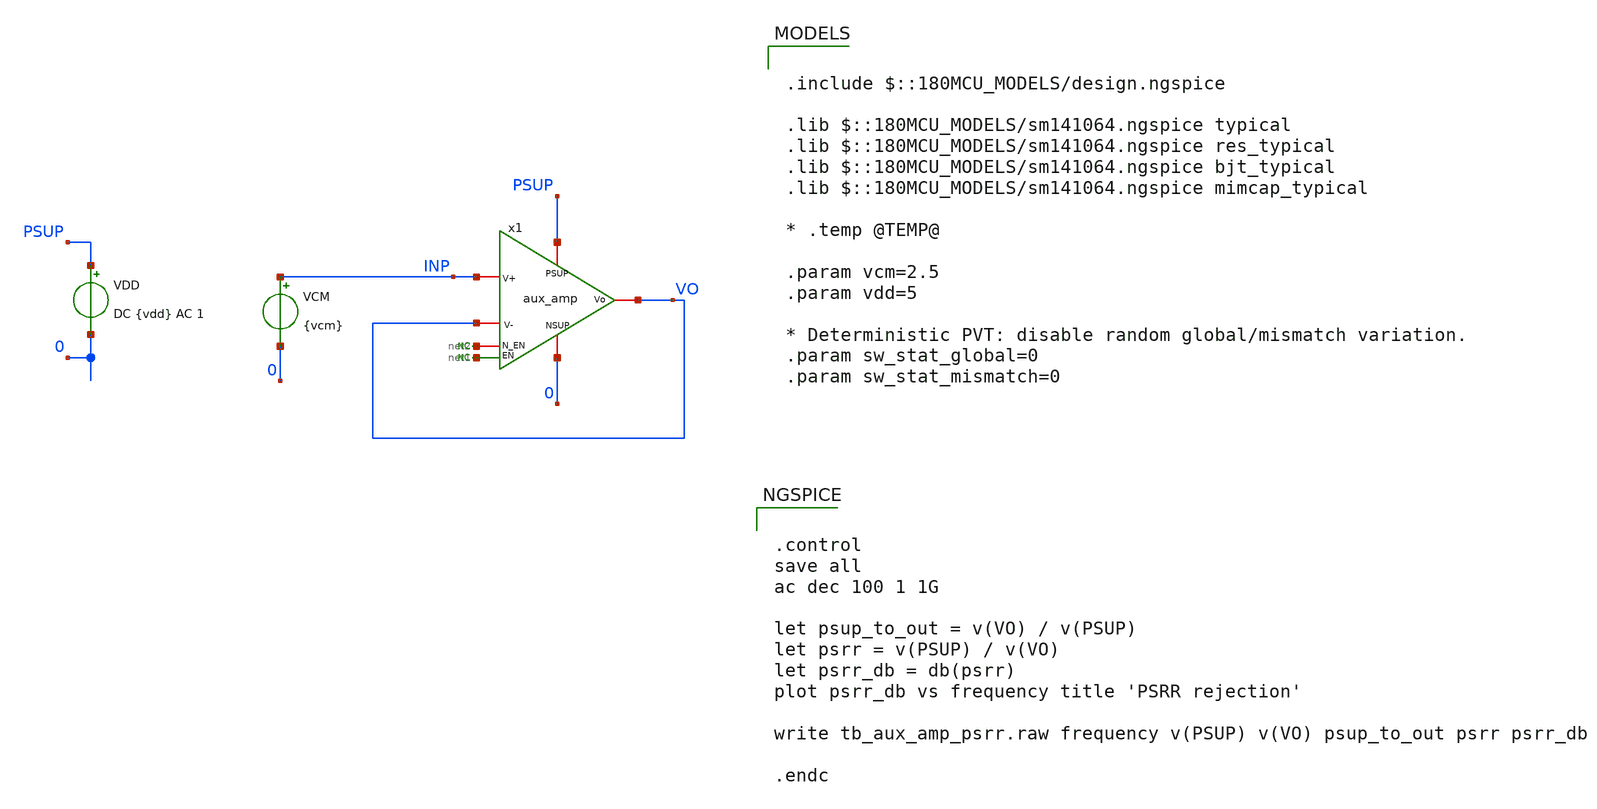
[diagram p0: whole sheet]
** sch_path: xschem/blocks/error_amp/tb_aux_amp_psrr.sch
**.subckt tb_aux_amp_psrr
VDD PSUP 0 DC {vdd} AC 1
VCM INP 0 {vcm}
* noconn #net1
* noconn #net2
x1 PSUP VO INP VO net2 0 net1 aux_amp
**** begin user architecture code

.include $::180MCU_MODELS/design.ngspice

.lib $::180MCU_MODELS/sm141064.ngspice typical
.lib $::180MCU_MODELS/sm141064.ngspice res_typical
.lib $::180MCU_MODELS/sm141064.ngspice bjt_typical
.lib $::180MCU_MODELS/sm141064.ngspice mimcap_typical

* .temp @TEMP@

.param vcm=2.5
.param vdd=5

* Deterministic PVT: disable random global/mismatch variation.
.param sw_stat_global=0
.param sw_stat_mismatch=0



.control
save all
ac dec 100 1 1G

let psup_to_out = v(VO) / v(PSUP)
let psrr = v(PSUP) / v(VO)
let psrr_db = db(psrr)
plot psrr_db vs frequency title 'PSRR rejection'

write tb_aux_amp_psrr.raw frequency v(PSUP) v(VO) psup_to_out psrr psrr_db

.endc


**** end user architecture code
**.ends

* expanding   symbol:  blocks/aux_amp/aux_amp.sym # of pins=7
** sym_path: xschem/lib/aux_amp.sym
** sch_path: xschem/lib/aux_amp.sch
.subckt aux_amp PSUP Vo V+ V- N_EN NSUP EN
*.ipin PSUP
*.ipin NSUP
*.ipin N_EN
*.ipin EN
*.ipin V+
*.ipin V-
*.opin Vo
XM1 Vo V- net2 net2 nfet_06v0 L=1.80u W=0.80u nf=1 ad='int((nf+1)/2) * W/nf * 0.18u' as='int((nf+2)/2) * W/nf * 0.18u'
+ pd='2*int((nf+1)/2) * (W/nf + 0.18u)' ps='2*int((nf+2)/2) * (W/nf + 0.18u)' nrd='0.18u / W' nrs='0.18u / W'
+ sa=0 sb=0 sd=0 m=1
XM2 net1 V+ net2 net2 nfet_06v0 L=1.80u W=0.80u nf=1 ad='int((nf+1)/2) * W/nf * 0.18u' as='int((nf+2)/2) * W/nf * 0.18u'
+ pd='2*int((nf+1)/2) * (W/nf + 0.18u)' ps='2*int((nf+2)/2) * (W/nf + 0.18u)' nrd='0.18u / W' nrs='0.18u / W'
+ sa=0 sb=0 sd=0 m=1
XM5 net1 net1 PSUP PSUP pfet_06v0 L=0.55u W=0.30u nf=1 ad='int((nf+1)/2) * W/nf * 0.18u' as='int((nf+2)/2) * W/nf * 0.18u'
+ pd='2*int((nf+1)/2) * (W/nf + 0.18u)' ps='2*int((nf+2)/2) * (W/nf + 0.18u)' nrd='0.18u / W' nrs='0.18u / W'
+ sa=0 sb=0 sd=0 m=1
XM6 Vo net1 PSUP PSUP pfet_06v0 L=0.55u W=0.30u nf=1 ad='int((nf+1)/2) * W/nf * 0.18u' as='int((nf+2)/2) * W/nf * 0.18u'
+ pd='2*int((nf+1)/2) * (W/nf + 0.18u)' ps='2*int((nf+2)/2) * (W/nf + 0.18u)' nrd='0.18u / W' nrs='0.18u / W'
+ sa=0 sb=0 sd=0 m=1
I0 net2 NSUP 5u
* noconn N_EN
* noconn EN
.ends

.end
